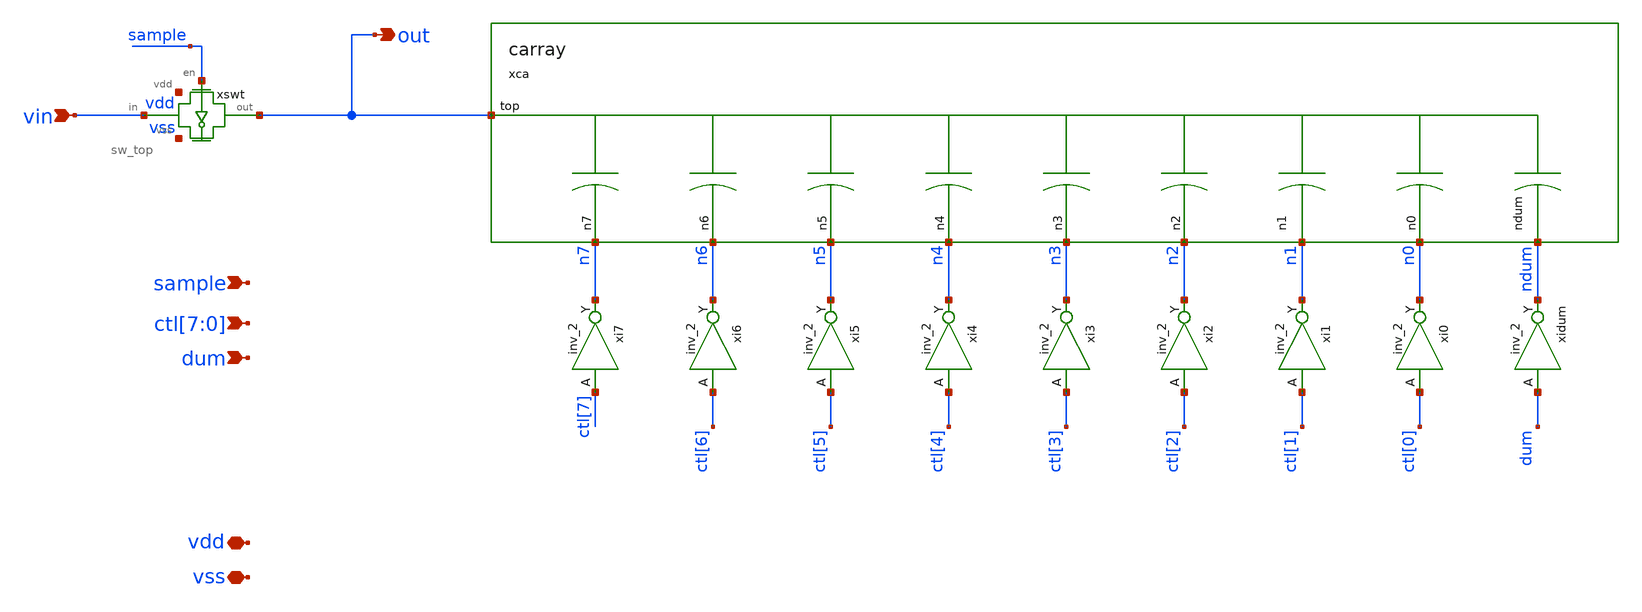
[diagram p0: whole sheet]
** sch_path: post_layout/sar/dac/dac.sch
**.subckt dac vin sample out ctl[7],ctl[6],ctl[5],ctl[4],ctl[3],ctl[2],ctl[1],ctl[0] dum vdd vss
*.ipin vin
*.ipin sample
*.opin out
*.ipin ctl[7],ctl[6],ctl[5],ctl[4],ctl[3],ctl[2],ctl[1],ctl[0]
*.ipin dum
*.iopin vdd
*.iopin vss
xca out n6 n0 n5 n4 n2 ndum n3 n1 n7 carray
xi6 ctl[6] vss vss vdd vdd n6 sky130_fd_sc_hd__inv_2
xi5 ctl[5] vss vss vdd vdd n5 sky130_fd_sc_hd__inv_2
xi4 ctl[4] vss vss vdd vdd n4 sky130_fd_sc_hd__inv_2
xi3 ctl[3] vss vss vdd vdd n3 sky130_fd_sc_hd__inv_2
xi2 ctl[2] vss vss vdd vdd n2 sky130_fd_sc_hd__inv_2
xi1 ctl[1] vss vss vdd vdd n1 sky130_fd_sc_hd__inv_2
xi0 ctl[0] vss vss vdd vdd n0 sky130_fd_sc_hd__inv_2
xidum dum vss vss vdd vdd ndum sky130_fd_sc_hd__inv_2
xi7 ctl[7] vss vss vdd vdd n7 sky130_fd_sc_hd__inv_2
xswt out sample vss vdd vin sw_top
**.ends
.end
